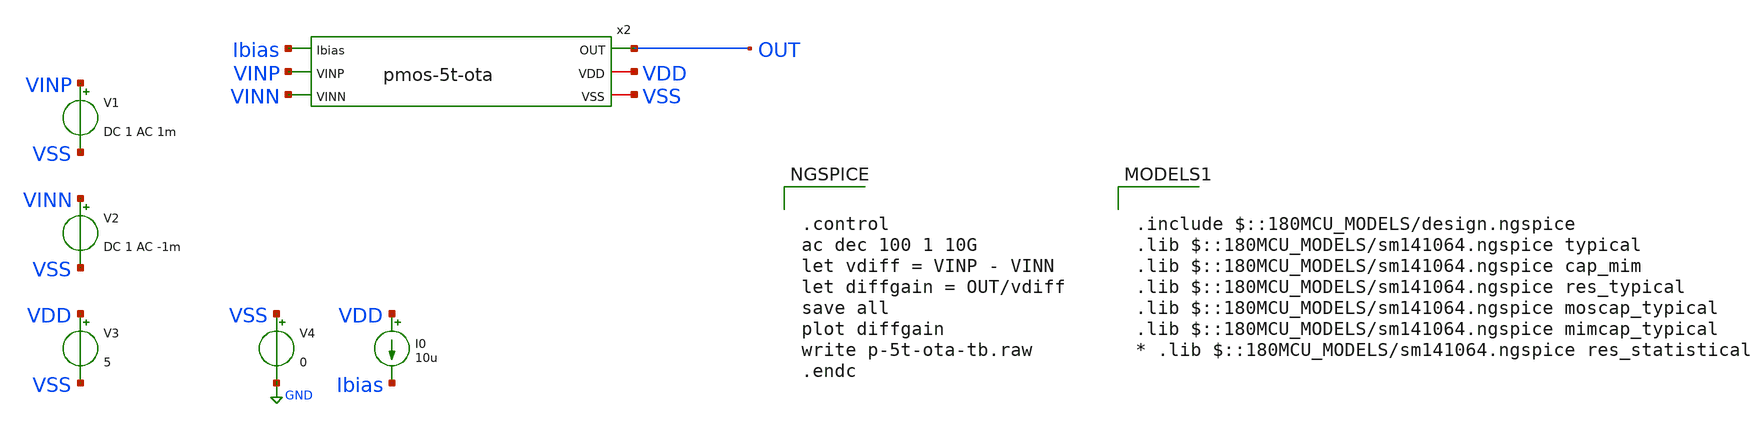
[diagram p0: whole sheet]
** sch_path: pmos-ota/pmos-5t-ota-tb.sch
**.subckt pmos-5t-ota-tb
V1 VINP VSS DC 1 AC 1m
V2 VINN VSS DC 1 AC -1m
V3 VDD VSS 5
V4 VSS GND 0
I0 VDD Ibias 10u
x2 Ibias VINP VINN OUT VDD VSS pmos-5t-ota
**** begin user architecture code


.control
ac dec 100 1 10G
let vdiff = VINP - VINN
let diffgain = OUT/vdiff
save all
plot diffgain
write p-5t-ota-tb.raw
.endc



.include $::180MCU_MODELS/design.ngspice
.lib $::180MCU_MODELS/sm141064.ngspice typical
.lib $::180MCU_MODELS/sm141064.ngspice cap_mim
.lib $::180MCU_MODELS/sm141064.ngspice res_typical
.lib $::180MCU_MODELS/sm141064.ngspice moscap_typical
.lib $::180MCU_MODELS/sm141064.ngspice mimcap_typical
* .lib $::180MCU_MODELS/sm141064.ngspice res_statistical

**** end user architecture code
**.ends

* expanding   symbol:  pmos-5t-ota.sym # of pins=6
** sym_path: pmos-ota/pmos-5t-ota.sym
** sch_path: pmos-ota/pmos-5t-ota.sch
.subckt pmos-5t-ota Ibias VINP VINN OUT VDD VSS
*.ipin Ibias
*.ipin VINP
*.ipin VINN
*.opin OUT
*.iopin VDD
*.iopin VSS
XM1 OUT VINN net2 VDD pfet_03v3 L=0.5u W=2u nf=1 ad='int((nf+1)/2) * W/nf * 0.18u' as='int((nf+2)/2) * W/nf * 0.18u'
+ pd='2*int((nf+1)/2) * (W/nf + 0.18u)' ps='2*int((nf+2)/2) * (W/nf + 0.18u)' nrd='0.18u / W' nrs='0.18u / W'
+ sa=0 sb=0 sd=0 m=1
XM2 net1 VINP net2 VDD pfet_03v3 L=0.5u W=2u nf=1 ad='int((nf+1)/2) * W/nf * 0.18u' as='int((nf+2)/2) * W/nf * 0.18u'
+ pd='2*int((nf+1)/2) * (W/nf + 0.18u)' ps='2*int((nf+2)/2) * (W/nf + 0.18u)' nrd='0.18u / W' nrs='0.18u / W'
+ sa=0 sb=0 sd=0 m=1
XM3 OUT net1 VSS VSS nfet_03v3 L=0.5u W=90u nf=1 ad='int((nf+1)/2) * W/nf * 0.18u' as='int((nf+2)/2) * W/nf * 0.18u'
+ pd='2*int((nf+1)/2) * (W/nf + 0.18u)' ps='2*int((nf+2)/2) * (W/nf + 0.18u)' nrd='0.18u / W' nrs='0.18u / W'
+ sa=0 sb=0 sd=0 m=1
XM4 net1 net1 VSS VSS nfet_03v3 L=0.5u W=90u nf=1 ad='int((nf+1)/2) * W/nf * 0.18u' as='int((nf+2)/2) * W/nf * 0.18u'
+ pd='2*int((nf+1)/2) * (W/nf + 0.18u)' ps='2*int((nf+2)/2) * (W/nf + 0.18u)' nrd='0.18u / W' nrs='0.18u / W'
+ sa=0 sb=0 sd=0 m=1
XM5 net2 Ibias VDD VDD pfet_03v3 L=2u W=10.5u nf=1 ad='int((nf+1)/2) * W/nf * 0.18u' as='int((nf+2)/2) * W/nf * 0.18u'
+ pd='2*int((nf+1)/2) * (W/nf + 0.18u)' ps='2*int((nf+2)/2) * (W/nf + 0.18u)' nrd='0.18u / W' nrs='0.18u / W'
+ sa=0 sb=0 sd=0 m=1
XM6 Ibias Ibias VDD VDD pfet_03v3 L=2u W=6.56u nf=1 ad='int((nf+1)/2) * W/nf * 0.18u' as='int((nf+2)/2) * W/nf * 0.18u'
+ pd='2*int((nf+1)/2) * (W/nf + 0.18u)' ps='2*int((nf+2)/2) * (W/nf + 0.18u)' nrd='0.18u / W' nrs='0.18u / W'
+ sa=0 sb=0 sd=0 m=1
.ends

.GLOBAL GND
.end
